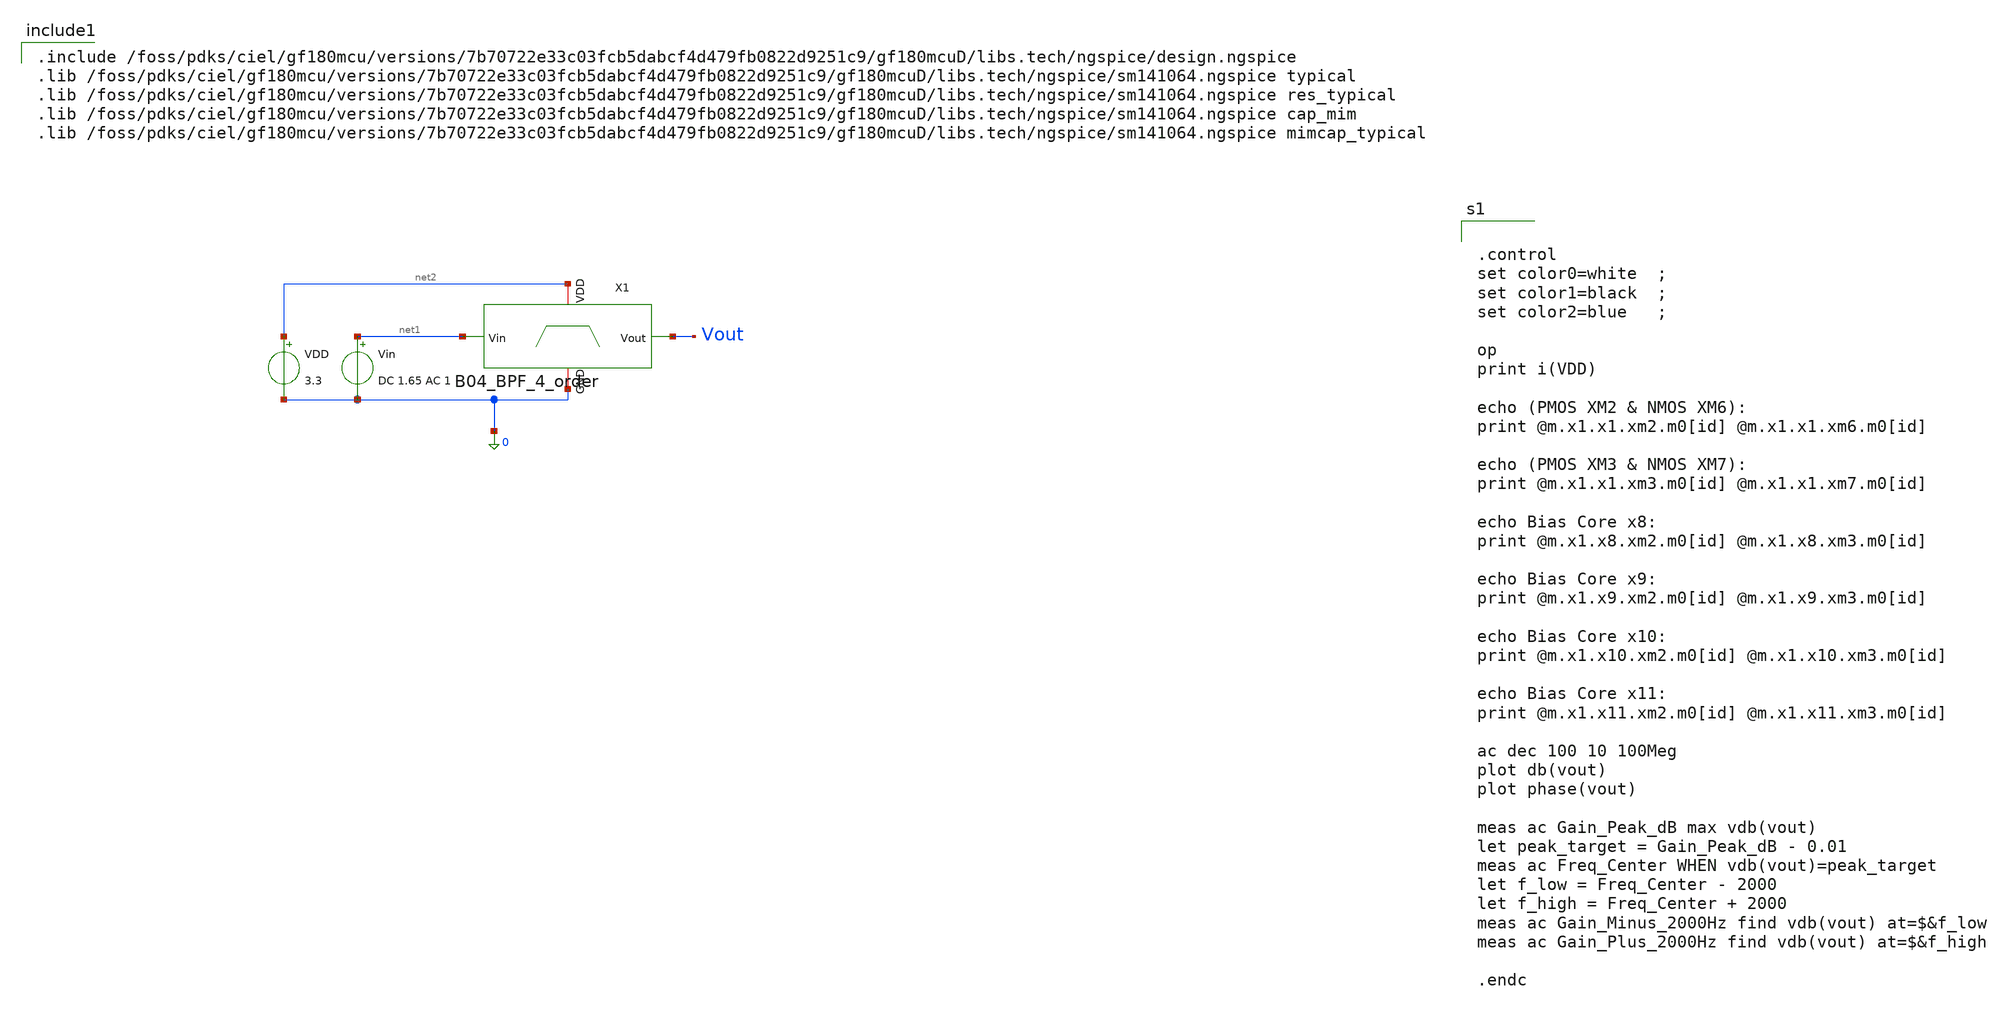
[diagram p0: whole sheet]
** sch_path: analog/B04_tb_BPF_4_order.sch
**.subckt B04_tb_BPF_4_order
Vin net1 0 DC 1.65 AC 1
VDD net2 0 3.3
X1 net2 Vout net1 0 B04_BPF_4_order
**** begin user architecture code

.include /foss/pdks/ciel/gf180mcu/versions/7b70722e33c03fcb5dabcf4d479fb0822d9251c9/gf180mcuD/libs.tech/ngspice/design.ngspice
.lib /foss/pdks/ciel/gf180mcu/versions/7b70722e33c03fcb5dabcf4d479fb0822d9251c9/gf180mcuD/libs.tech/ngspice/sm141064.ngspice typical
.lib /foss/pdks/ciel/gf180mcu/versions/7b70722e33c03fcb5dabcf4d479fb0822d9251c9/gf180mcuD/libs.tech/ngspice/sm141064.ngspice res_typical
.lib /foss/pdks/ciel/gf180mcu/versions/7b70722e33c03fcb5dabcf4d479fb0822d9251c9/gf180mcuD/libs.tech/ngspice/sm141064.ngspice cap_mim
.lib /foss/pdks/ciel/gf180mcu/versions/7b70722e33c03fcb5dabcf4d479fb0822d9251c9/gf180mcuD/libs.tech/ngspice/sm141064.ngspice mimcap_typical



.control
set color0=white  ;
set color1=black  ;
set color2=blue   ;

op
print i(VDD)

echo (PMOS XM2 & NMOS XM6):
print @m.x1.x1.xm2.m0[id] @m.x1.x1.xm6.m0[id]

echo (PMOS XM3 & NMOS XM7):
print @m.x1.x1.xm3.m0[id] @m.x1.x1.xm7.m0[id]

echo Bias Core x8:
print @m.x1.x8.xm2.m0[id] @m.x1.x8.xm3.m0[id]

echo Bias Core x9:
print @m.x1.x9.xm2.m0[id] @m.x1.x9.xm3.m0[id]

echo Bias Core x10:
print @m.x1.x10.xm2.m0[id] @m.x1.x10.xm3.m0[id]

echo Bias Core x11:
print @m.x1.x11.xm2.m0[id] @m.x1.x11.xm3.m0[id]

ac dec 100 10 100Meg
plot db(vout)
plot phase(vout)

meas ac Gain_Peak_dB max vdb(vout)
let peak_target = Gain_Peak_dB - 0.01
meas ac Freq_Center WHEN vdb(vout)=peak_target
let f_low = Freq_Center - 2000
let f_high = Freq_Center + 2000
meas ac Gain_Minus_2000Hz find vdb(vout) at=$&f_low
meas ac Gain_Plus_2000Hz find vdb(vout) at=$&f_high

.endc


**** end user architecture code
**.ends
.end
